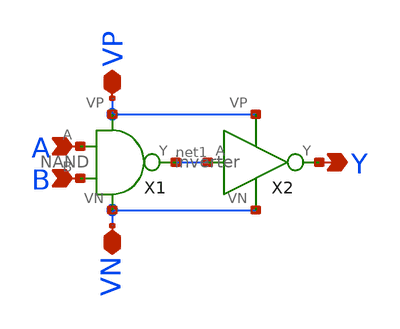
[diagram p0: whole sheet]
** sch_path: Homework1/AND.sch
**.subckt AND VP VN A B Y
*.iopin VP
*.iopin VN
*.ipin A
*.ipin B
*.opin Y
X1 A VP VN net1 B NAND
X2 net1 VP VN Y inverter
**.ends

* expanding   symbol:  /home/madvlsi/Documents/MADVLSI/Homework1/NAND.sym # of pins=5
** sym_path: Homework1/NAND.sym
** sch_path: Homework1/NAND.sch
.subckt NAND A VP VN Y B
*.ipin A
*.iopin VP
*.ipin B
*.iopin VN
*.opin Y
XM1 Y A net1 VN sky130_fd_pr__nfet_01v8 L=0.15 W=1 nf=1 ad='int((nf+1)/2) * W/nf * 0.29' as='int((nf+2)/2) * W/nf * 0.29'
+ pd='2*int((nf+1)/2) * (W/nf + 0.29)' ps='2*int((nf+2)/2) * (W/nf + 0.29)' nrd='0.29 / W' nrs='0.29 / W'
+ sa=0 sb=0 sd=0 mult=1 m=1
XM2 Y A VP VP sky130_fd_pr__pfet_01v8 L=0.15 W=1 nf=1 ad='int((nf+1)/2) * W/nf * 0.29' as='int((nf+2)/2) * W/nf * 0.29'
+ pd='2*int((nf+1)/2) * (W/nf + 0.29)' ps='2*int((nf+2)/2) * (W/nf + 0.29)' nrd='0.29 / W' nrs='0.29 / W'
+ sa=0 sb=0 sd=0 mult=1 m=1
XM6 Y B VP VP sky130_fd_pr__pfet_01v8 L=0.15 W=1 nf=1 ad='int((nf+1)/2) * W/nf * 0.29' as='int((nf+2)/2) * W/nf * 0.29'
+ pd='2*int((nf+1)/2) * (W/nf + 0.29)' ps='2*int((nf+2)/2) * (W/nf + 0.29)' nrd='0.29 / W' nrs='0.29 / W'
+ sa=0 sb=0 sd=0 mult=1 m=1
XM3 net1 B VN VN sky130_fd_pr__nfet_01v8 L=0.15 W=1 nf=1 ad='int((nf+1)/2) * W/nf * 0.29' as='int((nf+2)/2) * W/nf * 0.29'
+ pd='2*int((nf+1)/2) * (W/nf + 0.29)' ps='2*int((nf+2)/2) * (W/nf + 0.29)' nrd='0.29 / W' nrs='0.29 / W'
+ sa=0 sb=0 sd=0 mult=1 m=1
.ends


* expanding   symbol:  /home/madvlsi/Documents/MADVLSI/Homework1/inverter.sym # of pins=4
** sym_path: Homework1/inverter.sym
** sch_path: Homework1/inverter.sch
.subckt inverter A VP VN Y
*.ipin A
*.iopin VP
*.iopin VN
*.opin Y
XM1 Y A VN VN sky130_fd_pr__nfet_01v8 L=0.15 W=1 nf=1 ad='int((nf+1)/2) * W/nf * 0.29' as='int((nf+2)/2) * W/nf * 0.29'
+ pd='2*int((nf+1)/2) * (W/nf + 0.29)' ps='2*int((nf+2)/2) * (W/nf + 0.29)' nrd='0.29 / W' nrs='0.29 / W'
+ sa=0 sb=0 sd=0 mult=1 m=1
XM2 Y A VP VP sky130_fd_pr__pfet_01v8 L=0.15 W=1 nf=1 ad='int((nf+1)/2) * W/nf * 0.29' as='int((nf+2)/2) * W/nf * 0.29'
+ pd='2*int((nf+1)/2) * (W/nf + 0.29)' ps='2*int((nf+2)/2) * (W/nf + 0.29)' nrd='0.29 / W' nrs='0.29 / W'
+ sa=0 sb=0 sd=0 mult=1 m=1
.ends

.end
